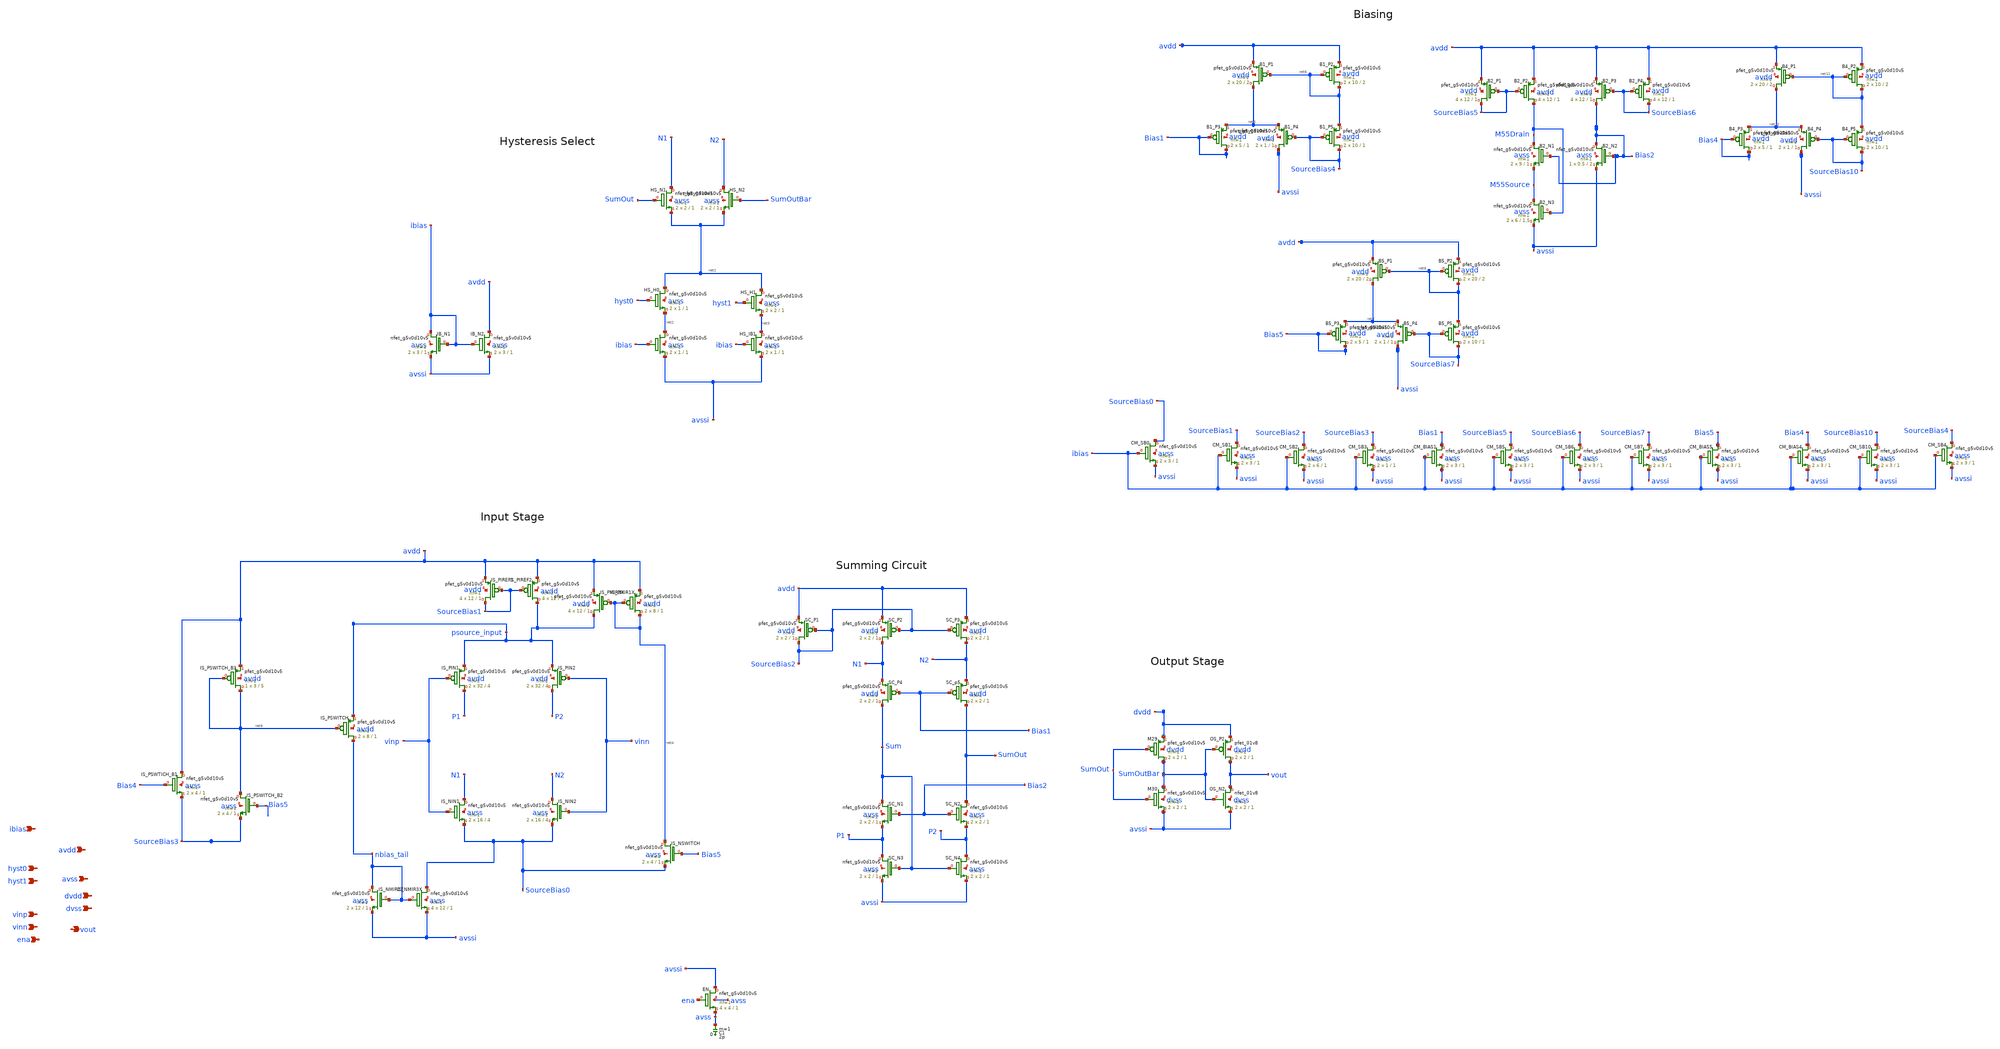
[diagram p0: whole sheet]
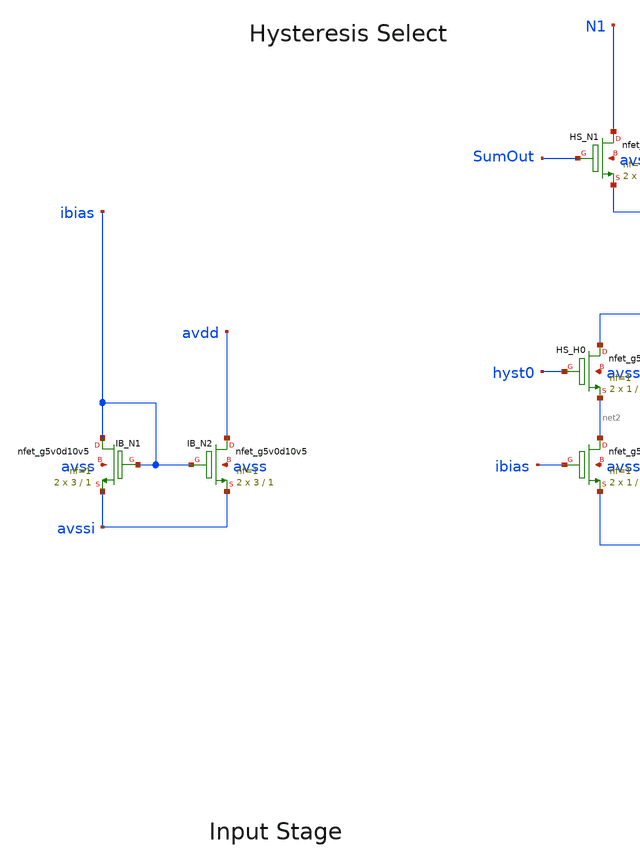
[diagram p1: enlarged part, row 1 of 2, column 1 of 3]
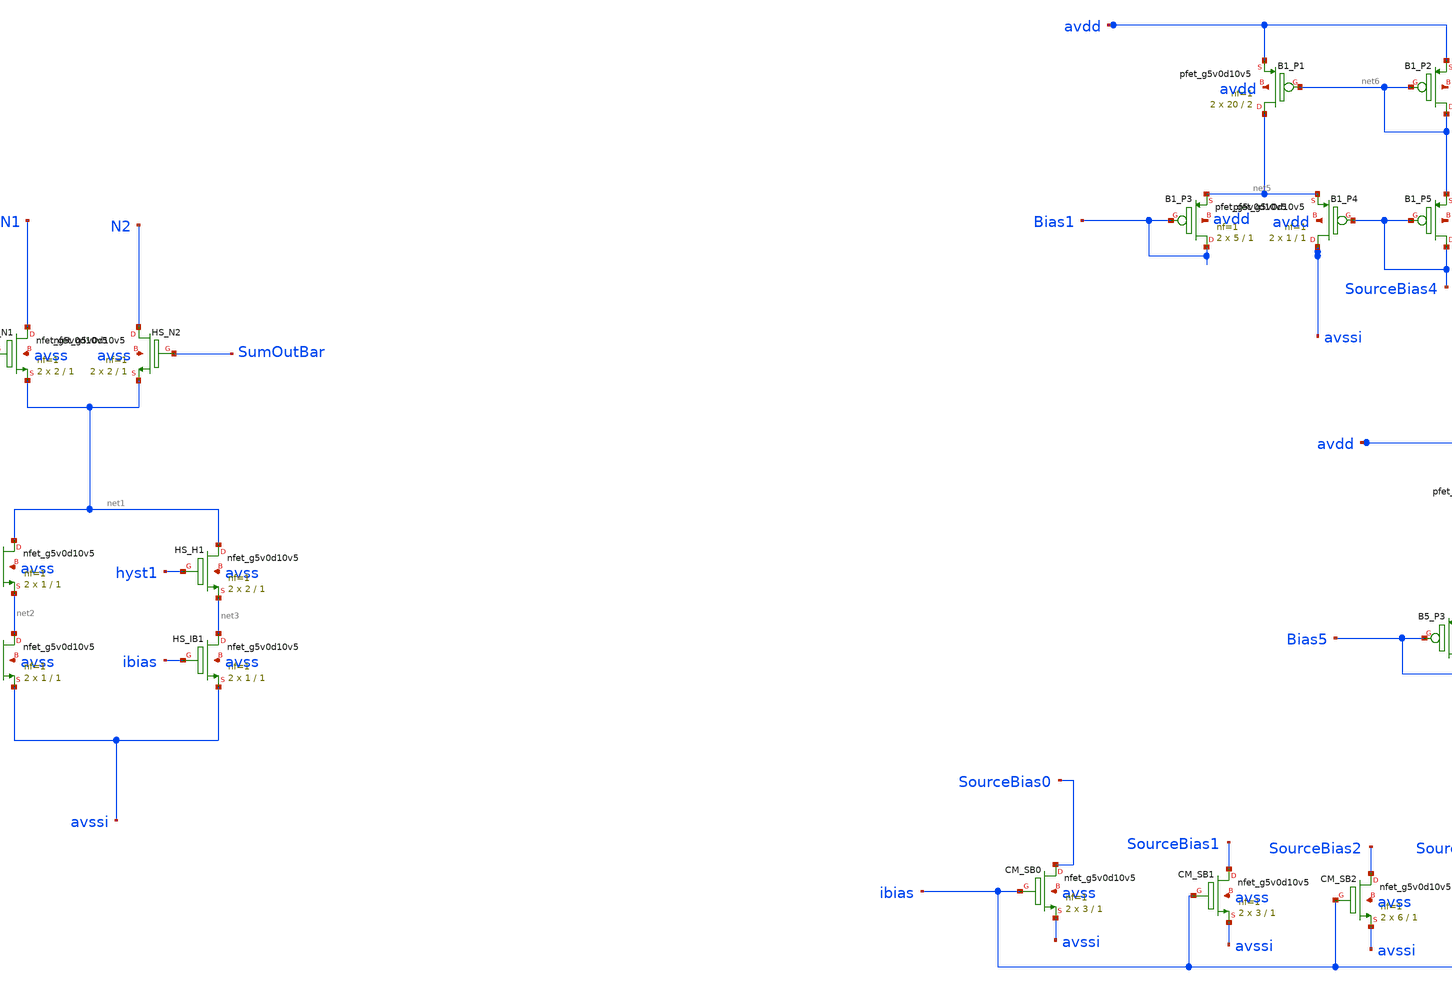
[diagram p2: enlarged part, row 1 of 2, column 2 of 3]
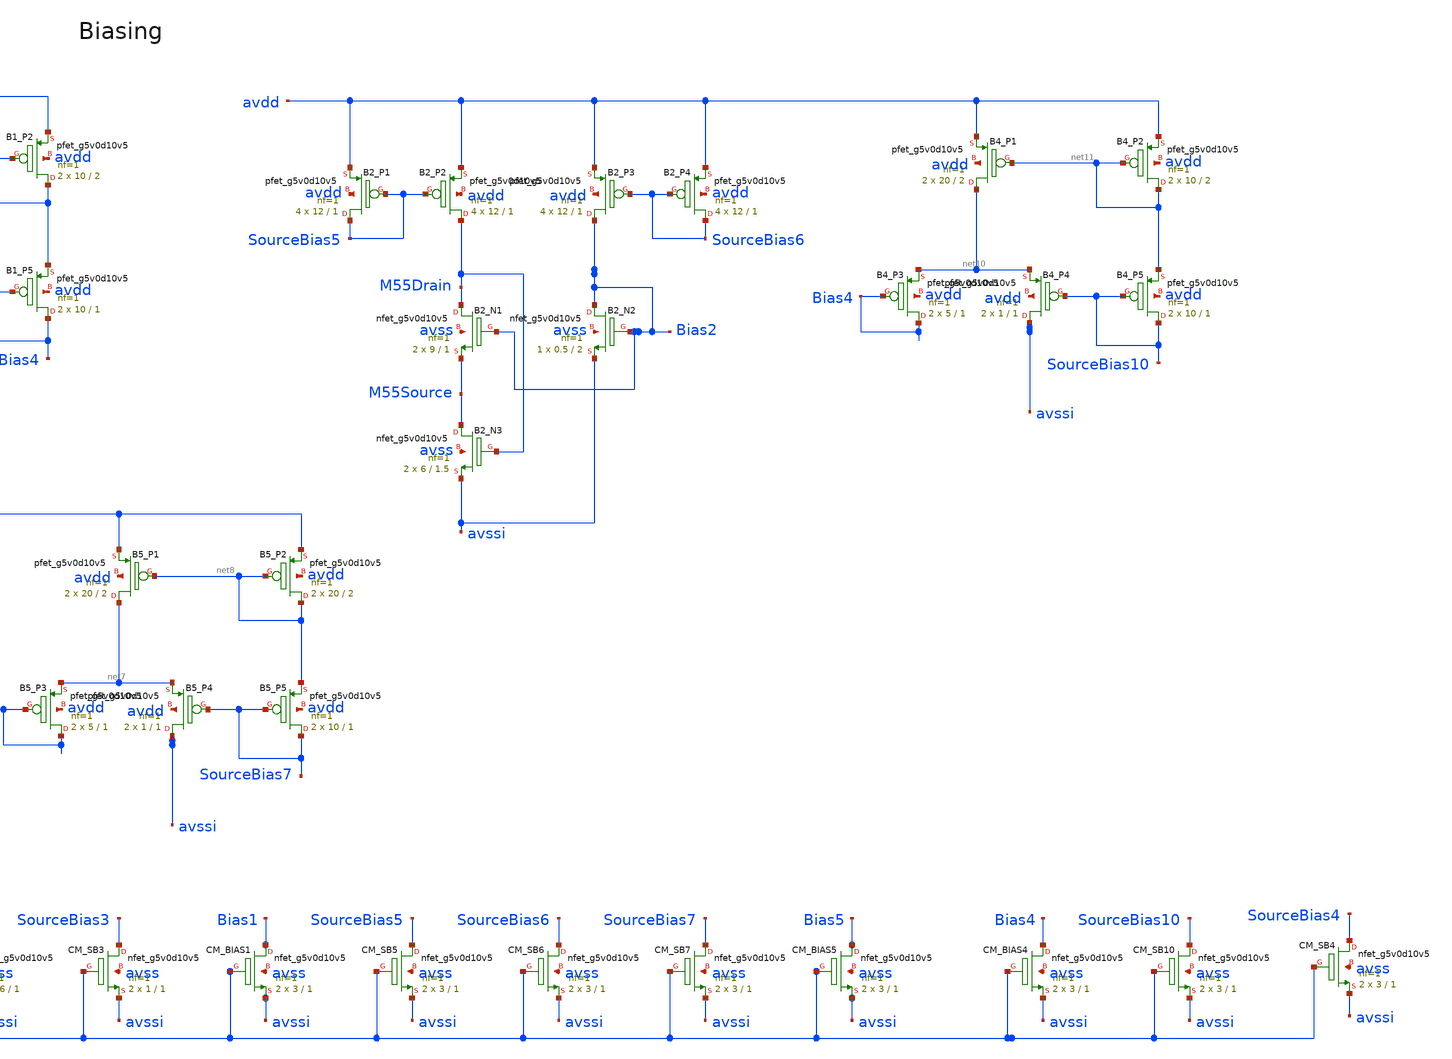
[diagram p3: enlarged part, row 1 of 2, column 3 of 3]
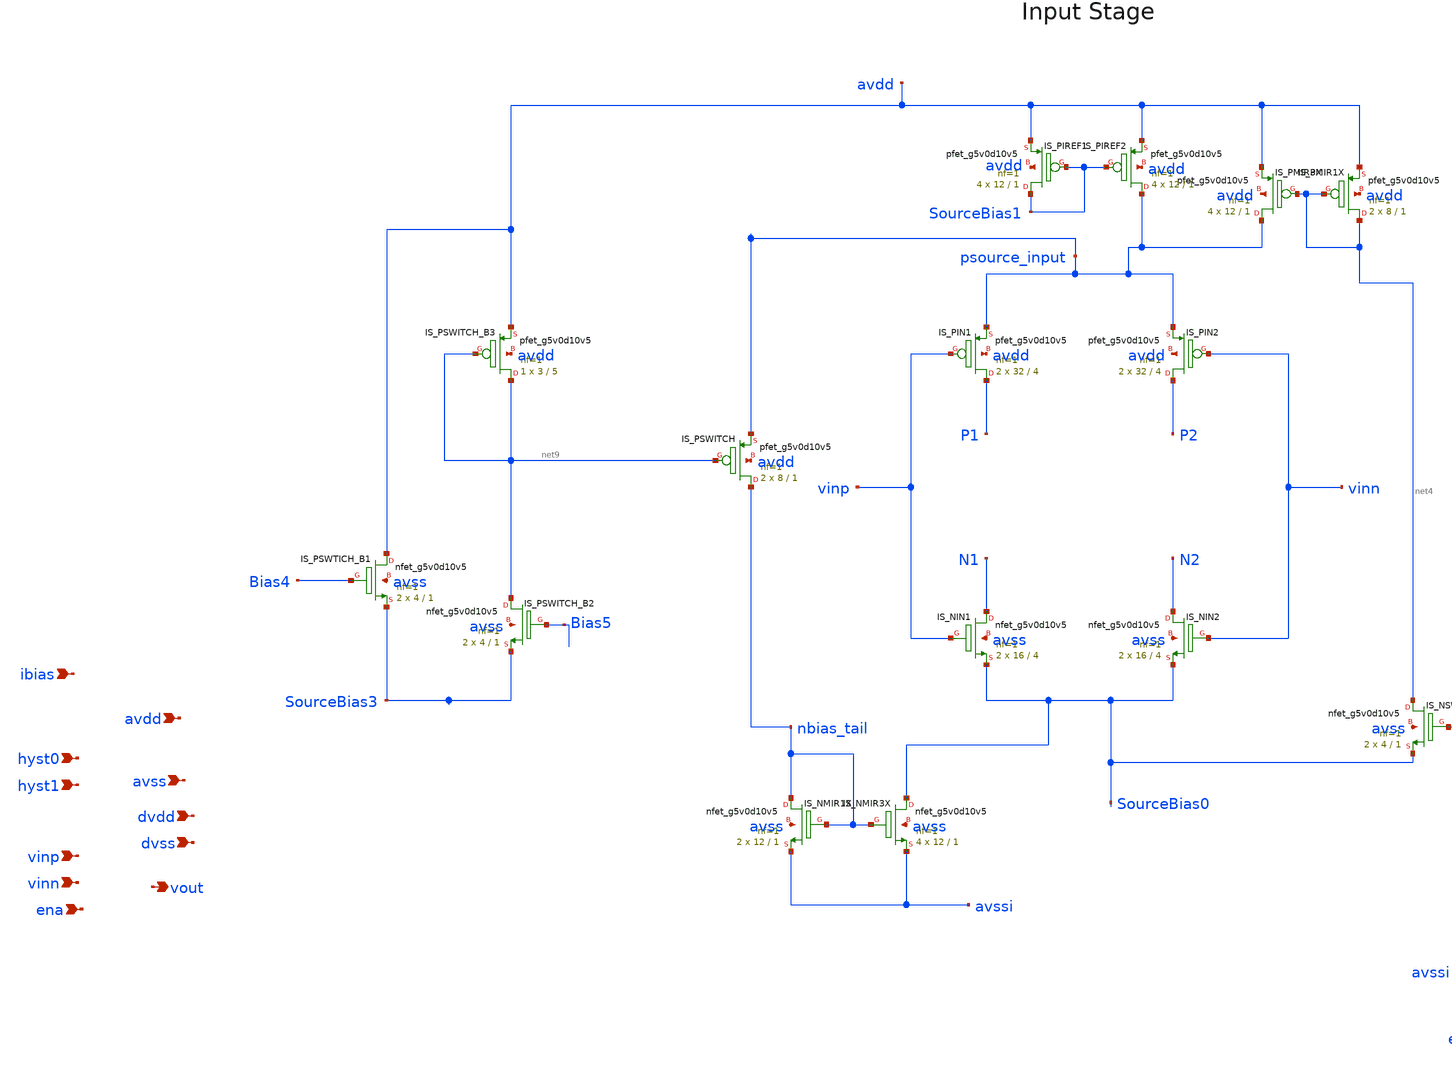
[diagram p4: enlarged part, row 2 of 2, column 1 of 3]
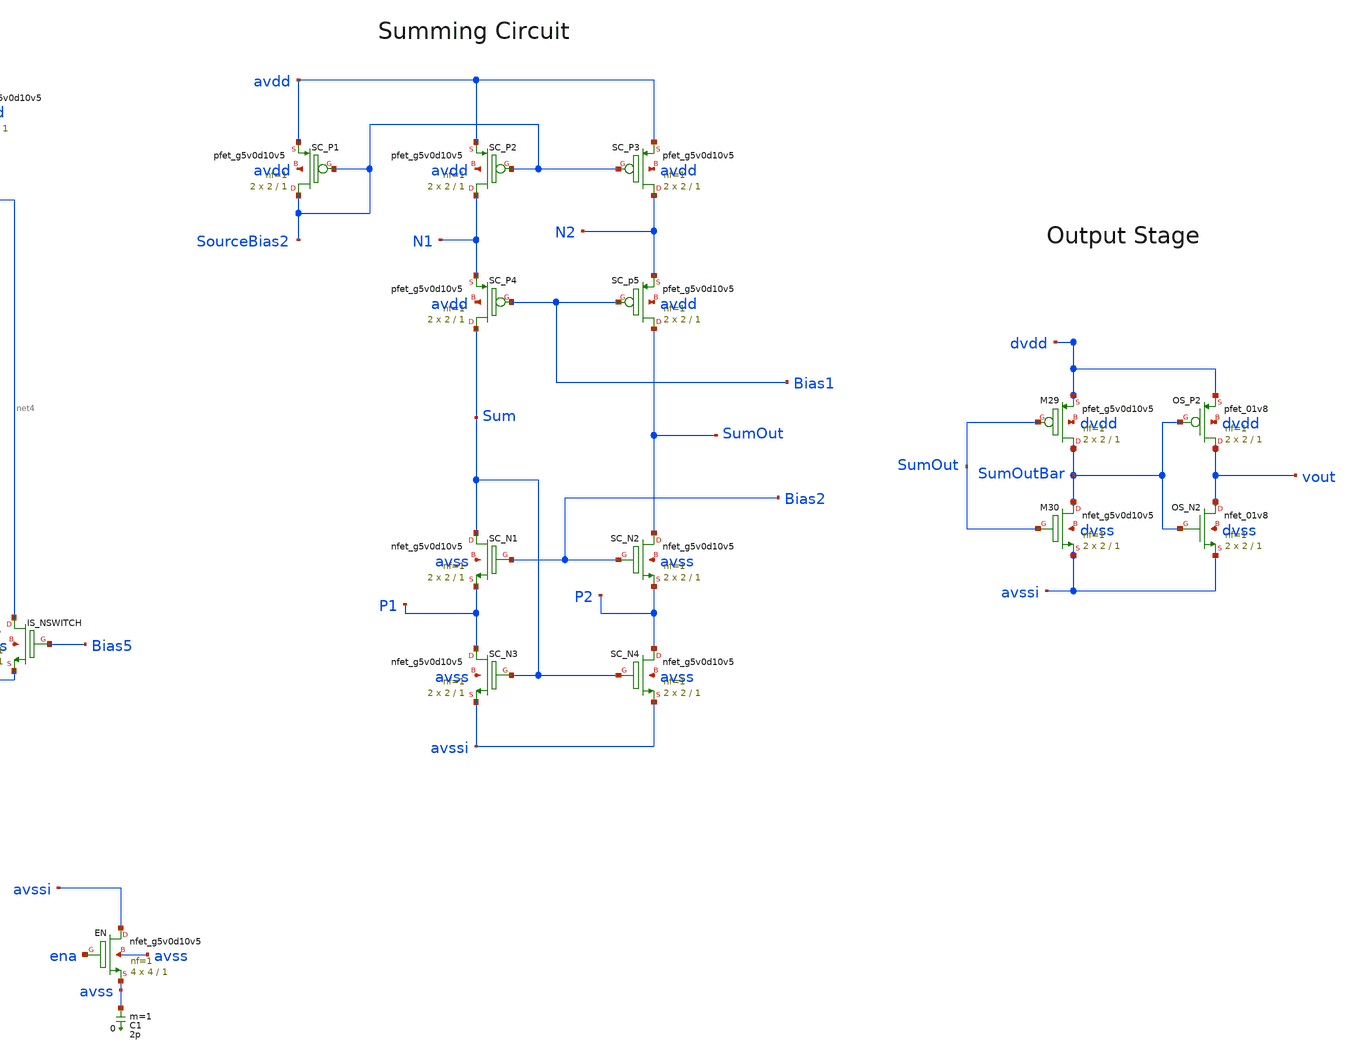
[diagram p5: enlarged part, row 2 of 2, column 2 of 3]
** sch_path: Chipalooza_April2024_Comparator/xschem/Chipalooza_April2024_Comparator.sch
**.subckt Chipalooza_April2024_Comparator vinp vinn hyst0 hyst1 avdd avss dvdd dvss vout ena ibias
*.ipin vinp
*.ipin vinn
*.ipin hyst0
*.ipin hyst1
*.ipin avdd
*.ipin avss
*.ipin dvdd
*.ipin dvss
*.opin vout
*.ipin ena
*.ipin ibias
C1 avss 0 2p m=1
XEN avssi ena avss avss sky130_fd_pr__nfet_g5v0d10v5 L=1 W=4 nf=1 ad='int((nf+1)/2) * W/nf * 0.29' as='int((nf+2)/2) * W/nf * 0.29'
+ pd='2*int((nf+1)/2) * (W/nf + 0.29)' ps='2*int((nf+2)/2) * (W/nf + 0.29)' nrd='0.29 / W' nrs='0.29 / W'
+ sa=0 sb=0 sd=0 mult=4 m=4
XHS_IB1 net3 ibias avssi avss sky130_fd_pr__nfet_g5v0d10v5 L=1 W=1 nf=1 ad='int((nf+1)/2) * W/nf * 0.29'
+ as='int((nf+2)/2) * W/nf * 0.29' pd='2*int((nf+1)/2) * (W/nf + 0.29)' ps='2*int((nf+2)/2) * (W/nf + 0.29)'
+ nrd='0.29 / W' nrs='0.29 / W' sa=0 sb=0 sd=0 mult=2 m=2
XOS_P2 vout SumOutBar dvdd dvdd sky130_fd_pr__pfet_01v8 L=1 W=2 nf=1 ad='int((nf+1)/2) * W/nf * 0.29'
+ as='int((nf+2)/2) * W/nf * 0.29' pd='2*int((nf+1)/2) * (W/nf + 0.29)' ps='2*int((nf+2)/2) * (W/nf + 0.29)'
+ nrd='0.29 / W' nrs='0.29 / W' sa=0 sb=0 sd=0 mult=2 m=2
XOS_N2 vout SumOutBar avssi dvss sky130_fd_pr__nfet_01v8 L=1 W=2 nf=1 ad='int((nf+1)/2) * W/nf * 0.29'
+ as='int((nf+2)/2) * W/nf * 0.29' pd='2*int((nf+1)/2) * (W/nf + 0.29)' ps='2*int((nf+2)/2) * (W/nf + 0.29)'
+ nrd='0.29 / W' nrs='0.29 / W' sa=0 sb=0 sd=0 mult=2 m=2
XSC_P1 SourceBias2 SourceBias2 avdd avdd sky130_fd_pr__pfet_g5v0d10v5 L=1 W=2 nf=1 ad='int((nf+1)/2) * W/nf * 0.29'
+ as='int((nf+2)/2) * W/nf * 0.29' pd='2*int((nf+1)/2) * (W/nf + 0.29)' ps='2*int((nf+2)/2) * (W/nf + 0.29)'
+ nrd='0.29 / W' nrs='0.29 / W' sa=0 sb=0 sd=0 mult=2 m=2
XSC_P2 N1 SourceBias2 avdd avdd sky130_fd_pr__pfet_g5v0d10v5 L=1 W=2 nf=1 ad='int((nf+1)/2) * W/nf * 0.29'
+ as='int((nf+2)/2) * W/nf * 0.29' pd='2*int((nf+1)/2) * (W/nf + 0.29)' ps='2*int((nf+2)/2) * (W/nf + 0.29)'
+ nrd='0.29 / W' nrs='0.29 / W' sa=0 sb=0 sd=0 mult=2 m=2
XSC_P3 N2 SourceBias2 avdd avdd sky130_fd_pr__pfet_g5v0d10v5 L=1 W=2 nf=1 ad='int((nf+1)/2) * W/nf * 0.29'
+ as='int((nf+2)/2) * W/nf * 0.29' pd='2*int((nf+1)/2) * (W/nf + 0.29)' ps='2*int((nf+2)/2) * (W/nf + 0.29)'
+ nrd='0.29 / W' nrs='0.29 / W' sa=0 sb=0 sd=0 mult=2 m=2
XSC_p5 SumOut Bias1 N2 avdd sky130_fd_pr__pfet_g5v0d10v5 L=1 W=2 nf=1 ad='int((nf+1)/2) * W/nf * 0.29'
+ as='int((nf+2)/2) * W/nf * 0.29' pd='2*int((nf+1)/2) * (W/nf + 0.29)' ps='2*int((nf+2)/2) * (W/nf + 0.29)'
+ nrd='0.29 / W' nrs='0.29 / W' sa=0 sb=0 sd=0 mult=2 m=2
XSC_P4 Sum Bias1 N1 avdd sky130_fd_pr__pfet_g5v0d10v5 L=1 W=2 nf=1 ad='int((nf+1)/2) * W/nf * 0.29' as='int((nf+2)/2) * W/nf * 0.29'
+ pd='2*int((nf+1)/2) * (W/nf + 0.29)' ps='2*int((nf+2)/2) * (W/nf + 0.29)' nrd='0.29 / W' nrs='0.29 / W'
+ sa=0 sb=0 sd=0 mult=2 m=2
XSC_N2 SumOut Bias2 P2 avss sky130_fd_pr__nfet_g5v0d10v5 L=1 W=2 nf=1 ad='int((nf+1)/2) * W/nf * 0.29'
+ as='int((nf+2)/2) * W/nf * 0.29' pd='2*int((nf+1)/2) * (W/nf + 0.29)' ps='2*int((nf+2)/2) * (W/nf + 0.29)'
+ nrd='0.29 / W' nrs='0.29 / W' sa=0 sb=0 sd=0 mult=2 m=2
XSC_N1 Sum Bias2 P1 avss sky130_fd_pr__nfet_g5v0d10v5 L=1 W=2 nf=1 ad='int((nf+1)/2) * W/nf * 0.29' as='int((nf+2)/2) * W/nf * 0.29'
+ pd='2*int((nf+1)/2) * (W/nf + 0.29)' ps='2*int((nf+2)/2) * (W/nf + 0.29)' nrd='0.29 / W' nrs='0.29 / W'
+ sa=0 sb=0 sd=0 mult=2 m=2
XSC_N4 P2 Sum avssi avss sky130_fd_pr__nfet_g5v0d10v5 L=1 W=2 nf=1 ad='int((nf+1)/2) * W/nf * 0.29' as='int((nf+2)/2) * W/nf * 0.29'
+ pd='2*int((nf+1)/2) * (W/nf + 0.29)' ps='2*int((nf+2)/2) * (W/nf + 0.29)' nrd='0.29 / W' nrs='0.29 / W'
+ sa=0 sb=0 sd=0 mult=2 m=2
XSC_N3 P1 Sum avssi avss sky130_fd_pr__nfet_g5v0d10v5 L=1 W=2 nf=1 ad='int((nf+1)/2) * W/nf * 0.29' as='int((nf+2)/2) * W/nf * 0.29'
+ pd='2*int((nf+1)/2) * (W/nf + 0.29)' ps='2*int((nf+2)/2) * (W/nf + 0.29)' nrd='0.29 / W' nrs='0.29 / W'
+ sa=0 sb=0 sd=0 mult=2 m=2
XIS_PIN2 P2 vinn psource_input avdd sky130_fd_pr__pfet_g5v0d10v5 L=4 W=32 nf=1 ad='int((nf+1)/2) * W/nf * 0.29'
+ as='int((nf+2)/2) * W/nf * 0.29' pd='2*int((nf+1)/2) * (W/nf + 0.29)' ps='2*int((nf+2)/2) * (W/nf + 0.29)'
+ nrd='0.29 / W' nrs='0.29 / W' sa=0 sb=0 sd=0 mult=2 m=2
XIS_PIN1 P1 vinp psource_input avdd sky130_fd_pr__pfet_g5v0d10v5 L=4 W=32 nf=1 ad='int((nf+1)/2) * W/nf * 0.29'
+ as='int((nf+2)/2) * W/nf * 0.29' pd='2*int((nf+1)/2) * (W/nf + 0.29)' ps='2*int((nf+2)/2) * (W/nf + 0.29)'
+ nrd='0.29 / W' nrs='0.29 / W' sa=0 sb=0 sd=0 mult=2 m=2
XIS_PMIR3X psource_input net4 avdd avdd sky130_fd_pr__pfet_g5v0d10v5 L=1 W=12 nf=1 ad='int((nf+1)/2) * W/nf * 0.29'
+ as='int((nf+2)/2) * W/nf * 0.29' pd='2*int((nf+1)/2) * (W/nf + 0.29)' ps='2*int((nf+2)/2) * (W/nf + 0.29)'
+ nrd='0.29 / W' nrs='0.29 / W' sa=0 sb=0 sd=0 mult=4 m=4
XIS_PMIR1X net4 net4 avdd avdd sky130_fd_pr__pfet_g5v0d10v5 L=1 W=8 nf=1 ad='int((nf+1)/2) * W/nf * 0.29'
+ as='int((nf+2)/2) * W/nf * 0.29' pd='2*int((nf+1)/2) * (W/nf + 0.29)' ps='2*int((nf+2)/2) * (W/nf + 0.29)'
+ nrd='0.29 / W' nrs='0.29 / W' sa=0 sb=0 sd=0 mult=2 m=2
XIS_PSWITCH nbias_tail net9 psource_input avdd sky130_fd_pr__pfet_g5v0d10v5 L=1 W=8 nf=1 ad='int((nf+1)/2) * W/nf * 0.29'
+ as='int((nf+2)/2) * W/nf * 0.29' pd='2*int((nf+1)/2) * (W/nf + 0.29)' ps='2*int((nf+2)/2) * (W/nf + 0.29)'
+ nrd='0.29 / W' nrs='0.29 / W' sa=0 sb=0 sd=0 mult=2 m=2
XIS_NIN1 N1 vinp SourceBias0 avss sky130_fd_pr__nfet_g5v0d10v5 L=4 W=16 nf=1 ad='int((nf+1)/2) * W/nf * 0.29'
+ as='int((nf+2)/2) * W/nf * 0.29' pd='2*int((nf+1)/2) * (W/nf + 0.29)' ps='2*int((nf+2)/2) * (W/nf + 0.29)'
+ nrd='0.29 / W' nrs='0.29 / W' sa=0 sb=0 sd=0 mult=2 m=2
XIS_NIN2 N2 vinn SourceBias0 avss sky130_fd_pr__nfet_g5v0d10v5 L=4 W=16 nf=1 ad='int((nf+1)/2) * W/nf * 0.29'
+ as='int((nf+2)/2) * W/nf * 0.29' pd='2*int((nf+1)/2) * (W/nf + 0.29)' ps='2*int((nf+2)/2) * (W/nf + 0.29)'
+ nrd='0.29 / W' nrs='0.29 / W' sa=0 sb=0 sd=0 mult=2 m=2
XIS_NMIR3X SourceBias0 nbias_tail avssi avss sky130_fd_pr__nfet_g5v0d10v5 L=1 W=12 nf=1 ad='int((nf+1)/2) * W/nf * 0.29'
+ as='int((nf+2)/2) * W/nf * 0.29' pd='2*int((nf+1)/2) * (W/nf + 0.29)' ps='2*int((nf+2)/2) * (W/nf + 0.29)'
+ nrd='0.29 / W' nrs='0.29 / W' sa=0 sb=0 sd=0 mult=4 m=4
XIS_NMIR1X nbias_tail nbias_tail avssi avss sky130_fd_pr__nfet_g5v0d10v5 L=1 W=12 nf=1 ad='int((nf+1)/2) * W/nf * 0.29'
+ as='int((nf+2)/2) * W/nf * 0.29' pd='2*int((nf+1)/2) * (W/nf + 0.29)' ps='2*int((nf+2)/2) * (W/nf + 0.29)'
+ nrd='0.29 / W' nrs='0.29 / W' sa=0 sb=0 sd=0 mult=2 m=2
XIS_NSWITCH net4 Bias5 SourceBias0 avss sky130_fd_pr__nfet_g5v0d10v5 L=1 W=4 nf=1 ad='int((nf+1)/2) * W/nf * 0.29'
+ as='int((nf+2)/2) * W/nf * 0.29' pd='2*int((nf+1)/2) * (W/nf + 0.29)' ps='2*int((nf+2)/2) * (W/nf + 0.29)'
+ nrd='0.29 / W' nrs='0.29 / W' sa=0 sb=0 sd=0 mult=2 m=2
XCM_SB1 SourceBias1 ibias avssi avss sky130_fd_pr__nfet_g5v0d10v5 L=1 W=3 nf=1 ad='int((nf+1)/2) * W/nf * 0.29'
+ as='int((nf+2)/2) * W/nf * 0.29' pd='2*int((nf+1)/2) * (W/nf + 0.29)' ps='2*int((nf+2)/2) * (W/nf + 0.29)'
+ nrd='0.29 / W' nrs='0.29 / W' sa=0 sb=0 sd=0 mult=2 m=2
XIS_PIREF1 SourceBias1 SourceBias1 avdd avdd sky130_fd_pr__pfet_g5v0d10v5 L=1 W=12 nf=1 ad='int((nf+1)/2) * W/nf * 0.29'
+ as='int((nf+2)/2) * W/nf * 0.29' pd='2*int((nf+1)/2) * (W/nf + 0.29)' ps='2*int((nf+2)/2) * (W/nf + 0.29)'
+ nrd='0.29 / W' nrs='0.29 / W' sa=0 sb=0 sd=0 mult=4 m=4
XIS_PIREF2 psource_input SourceBias1 avdd avdd sky130_fd_pr__pfet_g5v0d10v5 L=1 W=12 nf=1 ad='int((nf+1)/2) * W/nf * 0.29'
+ as='int((nf+2)/2) * W/nf * 0.29' pd='2*int((nf+1)/2) * (W/nf + 0.29)' ps='2*int((nf+2)/2) * (W/nf + 0.29)'
+ nrd='0.29 / W' nrs='0.29 / W' sa=0 sb=0 sd=0 mult=4 m=4
XCM_SB2 SourceBias2 ibias avssi avss sky130_fd_pr__nfet_g5v0d10v5 L=1 W=6 nf=1 ad='int((nf+1)/2) * W/nf * 0.29'
+ as='int((nf+2)/2) * W/nf * 0.29' pd='2*int((nf+1)/2) * (W/nf + 0.29)' ps='2*int((nf+2)/2) * (W/nf + 0.29)'
+ nrd='0.29 / W' nrs='0.29 / W' sa=0 sb=0 sd=0 mult=2 m=2
XCM_SB3 SourceBias3 ibias avssi avss sky130_fd_pr__nfet_g5v0d10v5 L=1 W=1 nf=1 ad='int((nf+1)/2) * W/nf * 0.29'
+ as='int((nf+2)/2) * W/nf * 0.29' pd='2*int((nf+1)/2) * (W/nf + 0.29)' ps='2*int((nf+2)/2) * (W/nf + 0.29)'
+ nrd='0.29 / W' nrs='0.29 / W' sa=0 sb=0 sd=0 mult=2 m=2
XCM_BIAS1 Bias1 ibias avssi avss sky130_fd_pr__nfet_g5v0d10v5 L=1 W=3 nf=1 ad='int((nf+1)/2) * W/nf * 0.29'
+ as='int((nf+2)/2) * W/nf * 0.29' pd='2*int((nf+1)/2) * (W/nf + 0.29)' ps='2*int((nf+2)/2) * (W/nf + 0.29)'
+ nrd='0.29 / W' nrs='0.29 / W' sa=0 sb=0 sd=0 mult=2 m=2
XCM_SB5 SourceBias5 ibias avssi avss sky130_fd_pr__nfet_g5v0d10v5 L=1 W=3 nf=1 ad='int((nf+1)/2) * W/nf * 0.29'
+ as='int((nf+2)/2) * W/nf * 0.29' pd='2*int((nf+1)/2) * (W/nf + 0.29)' ps='2*int((nf+2)/2) * (W/nf + 0.29)'
+ nrd='0.29 / W' nrs='0.29 / W' sa=0 sb=0 sd=0 mult=2 m=2
XCM_SB6 SourceBias6 ibias avssi avss sky130_fd_pr__nfet_g5v0d10v5 L=1 W=3 nf=1 ad='int((nf+1)/2) * W/nf * 0.29'
+ as='int((nf+2)/2) * W/nf * 0.29' pd='2*int((nf+1)/2) * (W/nf + 0.29)' ps='2*int((nf+2)/2) * (W/nf + 0.29)'
+ nrd='0.29 / W' nrs='0.29 / W' sa=0 sb=0 sd=0 mult=2 m=2
XCM_SB7 SourceBias7 ibias avssi avss sky130_fd_pr__nfet_g5v0d10v5 L=1 W=3 nf=1 ad='int((nf+1)/2) * W/nf * 0.29'
+ as='int((nf+2)/2) * W/nf * 0.29' pd='2*int((nf+1)/2) * (W/nf + 0.29)' ps='2*int((nf+2)/2) * (W/nf + 0.29)'
+ nrd='0.29 / W' nrs='0.29 / W' sa=0 sb=0 sd=0 mult=2 m=2
XCM_BIAS5 Bias5 ibias avssi avss sky130_fd_pr__nfet_g5v0d10v5 L=1 W=3 nf=1 ad='int((nf+1)/2) * W/nf * 0.29'
+ as='int((nf+2)/2) * W/nf * 0.29' pd='2*int((nf+1)/2) * (W/nf + 0.29)' ps='2*int((nf+2)/2) * (W/nf + 0.29)'
+ nrd='0.29 / W' nrs='0.29 / W' sa=0 sb=0 sd=0 mult=2 m=2
XB2_N3 M55Source M55Drain avssi avss sky130_fd_pr__nfet_g5v0d10v5 L=1.5 W=6 nf=1 ad='int((nf+1)/2) * W/nf * 0.29'
+ as='int((nf+2)/2) * W/nf * 0.29' pd='2*int((nf+1)/2) * (W/nf + 0.29)' ps='2*int((nf+2)/2) * (W/nf + 0.29)'
+ nrd='0.29 / W' nrs='0.29 / W' sa=0 sb=0 sd=0 mult=2 m=2
XB2_N1 M55Drain Bias2 M55Source avss sky130_fd_pr__nfet_g5v0d10v5 L=1 W=9 nf=1 ad='int((nf+1)/2) * W/nf * 0.29'
+ as='int((nf+2)/2) * W/nf * 0.29' pd='2*int((nf+1)/2) * (W/nf + 0.29)' ps='2*int((nf+2)/2) * (W/nf + 0.29)'
+ nrd='0.29 / W' nrs='0.29 / W' sa=0 sb=0 sd=0 mult=2 m=2
XB2_N2 Bias2 Bias2 avssi avss sky130_fd_pr__nfet_g5v0d10v5 L=2 W=0.5 nf=1 ad='int((nf+1)/2) * W/nf * 0.29'
+ as='int((nf+2)/2) * W/nf * 0.29' pd='2*int((nf+1)/2) * (W/nf + 0.29)' ps='2*int((nf+2)/2) * (W/nf + 0.29)'
+ nrd='0.29 / W' nrs='0.29 / W' sa=0 sb=0 sd=0 mult=1 m=1
XB1_P1 net5 net6 avdd avdd sky130_fd_pr__pfet_g5v0d10v5 L=2 W=20 nf=1 ad='int((nf+1)/2) * W/nf * 0.29'
+ as='int((nf+2)/2) * W/nf * 0.29' pd='2*int((nf+1)/2) * (W/nf + 0.29)' ps='2*int((nf+2)/2) * (W/nf + 0.29)'
+ nrd='0.29 / W' nrs='0.29 / W' sa=0 sb=0 sd=0 mult=2 m=2
XB1_P2 net6 net6 avdd avdd sky130_fd_pr__pfet_g5v0d10v5 L=2 W=10 nf=1 ad='int((nf+1)/2) * W/nf * 0.29'
+ as='int((nf+2)/2) * W/nf * 0.29' pd='2*int((nf+1)/2) * (W/nf + 0.29)' ps='2*int((nf+2)/2) * (W/nf + 0.29)'
+ nrd='0.29 / W' nrs='0.29 / W' sa=0 sb=0 sd=0 mult=2 m=2
XB1_P5 SourceBias4 SourceBias4 net6 avdd sky130_fd_pr__pfet_g5v0d10v5 L=1 W=10 nf=1 ad='int((nf+1)/2) * W/nf * 0.29'
+ as='int((nf+2)/2) * W/nf * 0.29' pd='2*int((nf+1)/2) * (W/nf + 0.29)' ps='2*int((nf+2)/2) * (W/nf + 0.29)'
+ nrd='0.29 / W' nrs='0.29 / W' sa=0 sb=0 sd=0 mult=2 m=2
XB1_P4 avssi SourceBias4 net5 avdd sky130_fd_pr__pfet_g5v0d10v5 L=1 W=1 nf=1 ad='int((nf+1)/2) * W/nf * 0.29'
+ as='int((nf+2)/2) * W/nf * 0.29' pd='2*int((nf+1)/2) * (W/nf + 0.29)' ps='2*int((nf+2)/2) * (W/nf + 0.29)'
+ nrd='0.29 / W' nrs='0.29 / W' sa=0 sb=0 sd=0 mult=2 m=2
XB1_P3 Bias1 Bias1 net5 avdd sky130_fd_pr__pfet_g5v0d10v5 L=1 W=5 nf=1 ad='int((nf+1)/2) * W/nf * 0.29'
+ as='int((nf+2)/2) * W/nf * 0.29' pd='2*int((nf+1)/2) * (W/nf + 0.29)' ps='2*int((nf+2)/2) * (W/nf + 0.29)'
+ nrd='0.29 / W' nrs='0.29 / W' sa=0 sb=0 sd=0 mult=2 m=2
XB5_P1 net7 net8 avdd avdd sky130_fd_pr__pfet_g5v0d10v5 L=2 W=20 nf=1 ad='int((nf+1)/2) * W/nf * 0.29'
+ as='int((nf+2)/2) * W/nf * 0.29' pd='2*int((nf+1)/2) * (W/nf + 0.29)' ps='2*int((nf+2)/2) * (W/nf + 0.29)'
+ nrd='0.29 / W' nrs='0.29 / W' sa=0 sb=0 sd=0 mult=2 m=2
XB5_P2 net8 net8 avdd avdd sky130_fd_pr__pfet_g5v0d10v5 L=2 W=20 nf=1 ad='int((nf+1)/2) * W/nf * 0.29'
+ as='int((nf+2)/2) * W/nf * 0.29' pd='2*int((nf+1)/2) * (W/nf + 0.29)' ps='2*int((nf+2)/2) * (W/nf + 0.29)'
+ nrd='0.29 / W' nrs='0.29 / W' sa=0 sb=0 sd=0 mult=2 m=2
XB5_P5 SourceBias7 SourceBias7 net8 avdd sky130_fd_pr__pfet_g5v0d10v5 L=1 W=10 nf=1 ad='int((nf+1)/2) * W/nf * 0.29'
+ as='int((nf+2)/2) * W/nf * 0.29' pd='2*int((nf+1)/2) * (W/nf + 0.29)' ps='2*int((nf+2)/2) * (W/nf + 0.29)'
+ nrd='0.29 / W' nrs='0.29 / W' sa=0 sb=0 sd=0 mult=2 m=2
XB5_P4 avssi SourceBias7 net7 avdd sky130_fd_pr__pfet_g5v0d10v5 L=1 W=1 nf=1 ad='int((nf+1)/2) * W/nf * 0.29'
+ as='int((nf+2)/2) * W/nf * 0.29' pd='2*int((nf+1)/2) * (W/nf + 0.29)' ps='2*int((nf+2)/2) * (W/nf + 0.29)'
+ nrd='0.29 / W' nrs='0.29 / W' sa=0 sb=0 sd=0 mult=2 m=2
XB5_P3 Bias5 Bias5 net7 avdd sky130_fd_pr__pfet_g5v0d10v5 L=1 W=5 nf=1 ad='int((nf+1)/2) * W/nf * 0.29'
+ as='int((nf+2)/2) * W/nf * 0.29' pd='2*int((nf+1)/2) * (W/nf + 0.29)' ps='2*int((nf+2)/2) * (W/nf + 0.29)'
+ nrd='0.29 / W' nrs='0.29 / W' sa=0 sb=0 sd=0 mult=2 m=2
XB2_P1 SourceBias5 SourceBias5 avdd avdd sky130_fd_pr__pfet_g5v0d10v5 L=1 W=12 nf=1 ad='int((nf+1)/2) * W/nf * 0.29'
+ as='int((nf+2)/2) * W/nf * 0.29' pd='2*int((nf+1)/2) * (W/nf + 0.29)' ps='2*int((nf+2)/2) * (W/nf + 0.29)'
+ nrd='0.29 / W' nrs='0.29 / W' sa=0 sb=0 sd=0 mult=4 m=4
XB2_P2 M55Drain SourceBias5 avdd avdd sky130_fd_pr__pfet_g5v0d10v5 L=1 W=12 nf=1 ad='int((nf+1)/2) * W/nf * 0.29'
+ as='int((nf+2)/2) * W/nf * 0.29' pd='2*int((nf+1)/2) * (W/nf + 0.29)' ps='2*int((nf+2)/2) * (W/nf + 0.29)'
+ nrd='0.29 / W' nrs='0.29 / W' sa=0 sb=0 sd=0 mult=4 m=4
XB2_P4 SourceBias6 SourceBias6 avdd avdd sky130_fd_pr__pfet_g5v0d10v5 L=1 W=12 nf=1 ad='int((nf+1)/2) * W/nf * 0.29'
+ as='int((nf+2)/2) * W/nf * 0.29' pd='2*int((nf+1)/2) * (W/nf + 0.29)' ps='2*int((nf+2)/2) * (W/nf + 0.29)'
+ nrd='0.29 / W' nrs='0.29 / W' sa=0 sb=0 sd=0 mult=4 m=4
XB2_P3 Bias2 SourceBias6 avdd avdd sky130_fd_pr__pfet_g5v0d10v5 L=1 W=12 nf=1 ad='int((nf+1)/2) * W/nf * 0.29'
+ as='int((nf+2)/2) * W/nf * 0.29' pd='2*int((nf+1)/2) * (W/nf + 0.29)' ps='2*int((nf+2)/2) * (W/nf + 0.29)'
+ nrd='0.29 / W' nrs='0.29 / W' sa=0 sb=0 sd=0 mult=4 m=4
XCM_SB0 SourceBias0 ibias avssi avss sky130_fd_pr__nfet_g5v0d10v5 L=1 W=3 nf=1 ad='int((nf+1)/2) * W/nf * 0.29'
+ as='int((nf+2)/2) * W/nf * 0.29' pd='2*int((nf+1)/2) * (W/nf + 0.29)' ps='2*int((nf+2)/2) * (W/nf + 0.29)'
+ nrd='0.29 / W' nrs='0.29 / W' sa=0 sb=0 sd=0 mult=2 m=2
XHS_N1 N1 SumOut net1 avss sky130_fd_pr__nfet_g5v0d10v5 L=1 W=2 nf=1 ad='int((nf+1)/2) * W/nf * 0.29'
+ as='int((nf+2)/2) * W/nf * 0.29' pd='2*int((nf+1)/2) * (W/nf + 0.29)' ps='2*int((nf+2)/2) * (W/nf + 0.29)'
+ nrd='0.29 / W' nrs='0.29 / W' sa=0 sb=0 sd=0 mult=2 m=2
XHS_N2 N2 SumOutBar net1 avss sky130_fd_pr__nfet_g5v0d10v5 L=1 W=2 nf=1 ad='int((nf+1)/2) * W/nf * 0.29'
+ as='int((nf+2)/2) * W/nf * 0.29' pd='2*int((nf+1)/2) * (W/nf + 0.29)' ps='2*int((nf+2)/2) * (W/nf + 0.29)'
+ nrd='0.29 / W' nrs='0.29 / W' sa=0 sb=0 sd=0 mult=2 m=2
XIB_N1 ibias ibias avssi avss sky130_fd_pr__nfet_g5v0d10v5 L=1 W=3 nf=1 ad='int((nf+1)/2) * W/nf * 0.29'
+ as='int((nf+2)/2) * W/nf * 0.29' pd='2*int((nf+1)/2) * (W/nf + 0.29)' ps='2*int((nf+2)/2) * (W/nf + 0.29)'
+ nrd='0.29 / W' nrs='0.29 / W' sa=0 sb=0 sd=0 mult=2 m=2
XIB_N2 avdd ibias avssi avss sky130_fd_pr__nfet_g5v0d10v5 L=1 W=3 nf=1 ad='int((nf+1)/2) * W/nf * 0.29'
+ as='int((nf+2)/2) * W/nf * 0.29' pd='2*int((nf+1)/2) * (W/nf + 0.29)' ps='2*int((nf+2)/2) * (W/nf + 0.29)'
+ nrd='0.29 / W' nrs='0.29 / W' sa=0 sb=0 sd=0 mult=2 m=2
XIS_PSWITCH_B3 net9 net9 avdd avdd sky130_fd_pr__pfet_g5v0d10v5 L=5 W=3 nf=1 ad='int((nf+1)/2) * W/nf * 0.29'
+ as='int((nf+2)/2) * W/nf * 0.29' pd='2*int((nf+1)/2) * (W/nf + 0.29)' ps='2*int((nf+2)/2) * (W/nf + 0.29)'
+ nrd='0.29 / W' nrs='0.29 / W' sa=0 sb=0 sd=0 mult=1 m=1
XIS_PSWTICH_B1 avdd Bias4 SourceBias3 avss sky130_fd_pr__nfet_g5v0d10v5 L=1 W=4 nf=1 ad='int((nf+1)/2) * W/nf * 0.29'
+ as='int((nf+2)/2) * W/nf * 0.29' pd='2*int((nf+1)/2) * (W/nf + 0.29)' ps='2*int((nf+2)/2) * (W/nf + 0.29)'
+ nrd='0.29 / W' nrs='0.29 / W' sa=0 sb=0 sd=0 mult=2 m=2
XIS_PSWITCH_B2 net9 Bias5 SourceBias3 avss sky130_fd_pr__nfet_g5v0d10v5 L=1 W=4 nf=1 ad='int((nf+1)/2) * W/nf * 0.29'
+ as='int((nf+2)/2) * W/nf * 0.29' pd='2*int((nf+1)/2) * (W/nf + 0.29)' ps='2*int((nf+2)/2) * (W/nf + 0.29)'
+ nrd='0.29 / W' nrs='0.29 / W' sa=0 sb=0 sd=0 mult=2 m=2
XB4_P1 net10 net11 avdd avdd sky130_fd_pr__pfet_g5v0d10v5 L=2 W=20 nf=1 ad='int((nf+1)/2) * W/nf * 0.29'
+ as='int((nf+2)/2) * W/nf * 0.29' pd='2*int((nf+1)/2) * (W/nf + 0.29)' ps='2*int((nf+2)/2) * (W/nf + 0.29)'
+ nrd='0.29 / W' nrs='0.29 / W' sa=0 sb=0 sd=0 mult=2 m=2
XB4_P2 net11 net11 avdd avdd sky130_fd_pr__pfet_g5v0d10v5 L=2 W=10 nf=1 ad='int((nf+1)/2) * W/nf * 0.29'
+ as='int((nf+2)/2) * W/nf * 0.29' pd='2*int((nf+1)/2) * (W/nf + 0.29)' ps='2*int((nf+2)/2) * (W/nf + 0.29)'
+ nrd='0.29 / W' nrs='0.29 / W' sa=0 sb=0 sd=0 mult=2 m=2
XB4_P5 SourceBias10 SourceBias10 net11 avdd sky130_fd_pr__pfet_g5v0d10v5 L=1 W=10 nf=1 ad='int((nf+1)/2) * W/nf * 0.29'
+ as='int((nf+2)/2) * W/nf * 0.29' pd='2*int((nf+1)/2) * (W/nf + 0.29)' ps='2*int((nf+2)/2) * (W/nf + 0.29)'
+ nrd='0.29 / W' nrs='0.29 / W' sa=0 sb=0 sd=0 mult=2 m=2
XM1 net2 ibias avssi avss sky130_fd_pr__nfet_g5v0d10v5 L=1 W=1 nf=1 ad='int((nf+1)/2) * W/nf * 0.29'
+ as='int((nf+2)/2) * W/nf * 0.29' pd='2*int((nf+1)/2) * (W/nf + 0.29)' ps='2*int((nf+2)/2) * (W/nf + 0.29)'
+ nrd='0.29 / W' nrs='0.29 / W' sa=0 sb=0 sd=0 mult=2 m=2
XHS_H0 net1 hyst0 net2 avss sky130_fd_pr__nfet_g5v0d10v5 L=1 W=1 nf=1 ad='int((nf+1)/2) * W/nf * 0.29'
+ as='int((nf+2)/2) * W/nf * 0.29' pd='2*int((nf+1)/2) * (W/nf + 0.29)' ps='2*int((nf+2)/2) * (W/nf + 0.29)'
+ nrd='0.29 / W' nrs='0.29 / W' sa=0 sb=0 sd=0 mult=2 m=2
XHS_H1 net1 hyst1 net3 avss sky130_fd_pr__nfet_g5v0d10v5 L=1 W=2 nf=1 ad='int((nf+1)/2) * W/nf * 0.29'
+ as='int((nf+2)/2) * W/nf * 0.29' pd='2*int((nf+1)/2) * (W/nf + 0.29)' ps='2*int((nf+2)/2) * (W/nf + 0.29)'
+ nrd='0.29 / W' nrs='0.29 / W' sa=0 sb=0 sd=0 mult=2 m=2
XCM_BIAS4 Bias4 ibias avssi avss sky130_fd_pr__nfet_g5v0d10v5 L=1 W=3 nf=1 ad='int((nf+1)/2) * W/nf * 0.29'
+ as='int((nf+2)/2) * W/nf * 0.29' pd='2*int((nf+1)/2) * (W/nf + 0.29)' ps='2*int((nf+2)/2) * (W/nf + 0.29)'
+ nrd='0.29 / W' nrs='0.29 / W' sa=0 sb=0 sd=0 mult=2 m=2
XCM_SB10 SourceBias10 ibias avssi avss sky130_fd_pr__nfet_g5v0d10v5 L=1 W=3 nf=1 ad='int((nf+1)/2) * W/nf * 0.29'
+ as='int((nf+2)/2) * W/nf * 0.29' pd='2*int((nf+1)/2) * (W/nf + 0.29)' ps='2*int((nf+2)/2) * (W/nf + 0.29)'
+ nrd='0.29 / W' nrs='0.29 / W' sa=0 sb=0 sd=0 mult=2 m=2
XCM_SB4 SourceBias4 ibias avssi avss sky130_fd_pr__nfet_g5v0d10v5 L=1 W=3 nf=1 ad='int((nf+1)/2) * W/nf * 0.29'
+ as='int((nf+2)/2) * W/nf * 0.29' pd='2*int((nf+1)/2) * (W/nf + 0.29)' ps='2*int((nf+2)/2) * (W/nf + 0.29)'
+ nrd='0.29 / W' nrs='0.29 / W' sa=0 sb=0 sd=0 mult=2 m=2
XB4_P4 avssi SourceBias10 net10 avdd sky130_fd_pr__pfet_g5v0d10v5 L=1 W=1 nf=1 ad='int((nf+1)/2) * W/nf * 0.29'
+ as='int((nf+2)/2) * W/nf * 0.29' pd='2*int((nf+1)/2) * (W/nf + 0.29)' ps='2*int((nf+2)/2) * (W/nf + 0.29)'
+ nrd='0.29 / W' nrs='0.29 / W' sa=0 sb=0 sd=0 mult=2 m=2
XB4_P3 Bias4 Bias4 net10 avdd sky130_fd_pr__pfet_g5v0d10v5 L=1 W=5 nf=1 ad='int((nf+1)/2) * W/nf * 0.29'
+ as='int((nf+2)/2) * W/nf * 0.29' pd='2*int((nf+1)/2) * (W/nf + 0.29)' ps='2*int((nf+2)/2) * (W/nf + 0.29)'
+ nrd='0.29 / W' nrs='0.29 / W' sa=0 sb=0 sd=0 mult=2 m=2
XM29 SumOutBar SumOut dvdd dvdd sky130_fd_pr__pfet_g5v0d10v5 L=1 W=2 nf=1 ad='int((nf+1)/2) * W/nf * 0.29'
+ as='int((nf+2)/2) * W/nf * 0.29' pd='2*int((nf+1)/2) * (W/nf + 0.29)' ps='2*int((nf+2)/2) * (W/nf + 0.29)'
+ nrd='0.29 / W' nrs='0.29 / W' sa=0 sb=0 sd=0 mult=2 m=2
XM30 SumOutBar SumOut avssi dvss sky130_fd_pr__nfet_g5v0d10v5 L=1 W=2 nf=1 ad='int((nf+1)/2) * W/nf * 0.29'
+ as='int((nf+2)/2) * W/nf * 0.29' pd='2*int((nf+1)/2) * (W/nf + 0.29)' ps='2*int((nf+2)/2) * (W/nf + 0.29)'
+ nrd='0.29 / W' nrs='0.29 / W' sa=0 sb=0 sd=0 mult=2 m=2
**.ends
.end
